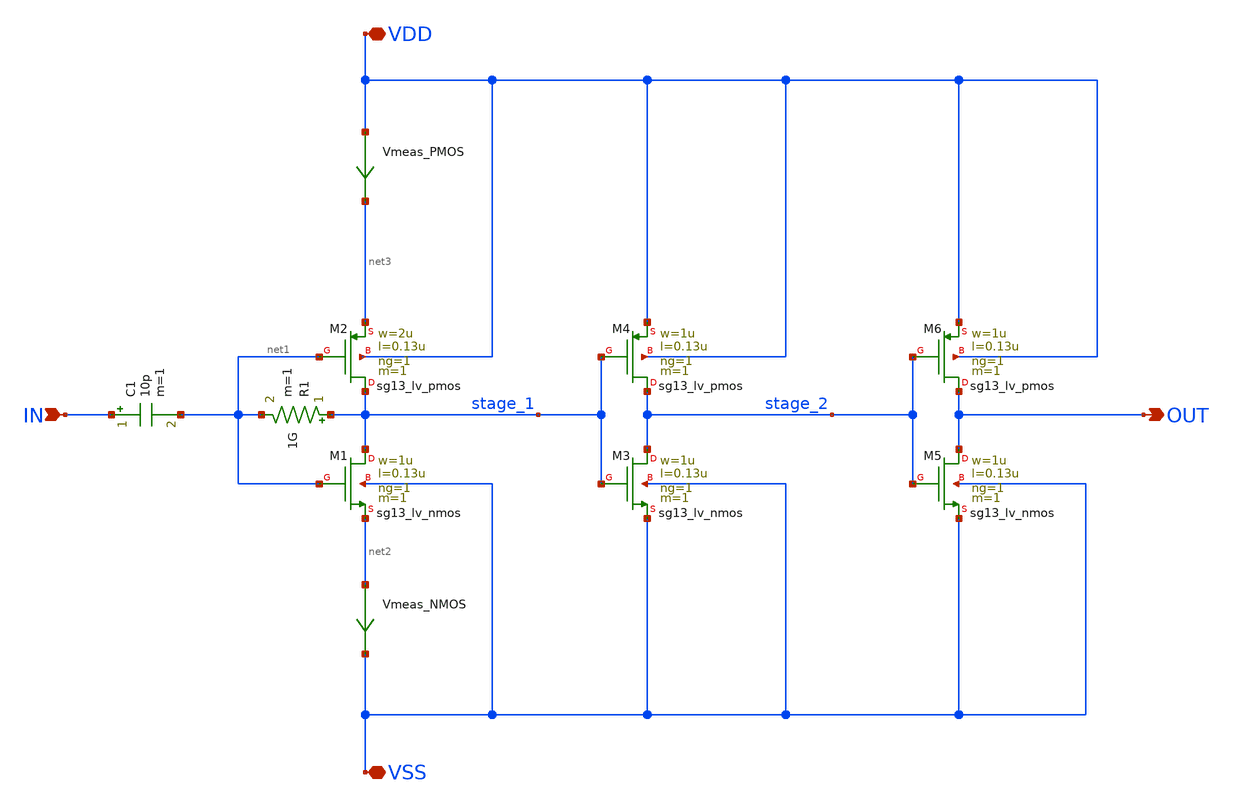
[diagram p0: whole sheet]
** sch_path: clock_gen_v1.sch
**.subckt clock_gen_v1 VSS VDD IN OUT
*.iopin VSS
*.iopin VDD
*.ipin IN
*.opin OUT
XM1 stage_1 net1 net2 VSS sg13_lv_nmos w=1u l=0.13u ng=1 m=1 mm_ok=1
XM2 stage_1 net1 net3 VDD sg13_lv_pmos w=2u l=0.13u ng=1 m=1 mm_ok=1
R1 stage_1 net1 1G m=1
C1 IN net1 10p m=1
XM3 stage_2 stage_1 VSS VSS sg13_lv_nmos w=1u l=0.13u ng=1 m=1 mm_ok=1
XM4 stage_2 stage_1 VDD VDD sg13_lv_pmos w=1u l=0.13u ng=1 m=1 mm_ok=1
XM5 OUT stage_2 VSS VSS sg13_lv_nmos w=1u l=0.13u ng=1 m=1 mm_ok=1
XM6 OUT stage_2 VDD VDD sg13_lv_pmos w=1u l=0.13u ng=1 m=1 mm_ok=1
Vmeas_NMOS net2 VSS 0
.save i(vmeas_nmos)
Vmeas_PMOS net4 net3 0
.save i(vmeas_pmos)
**.ends
.end
